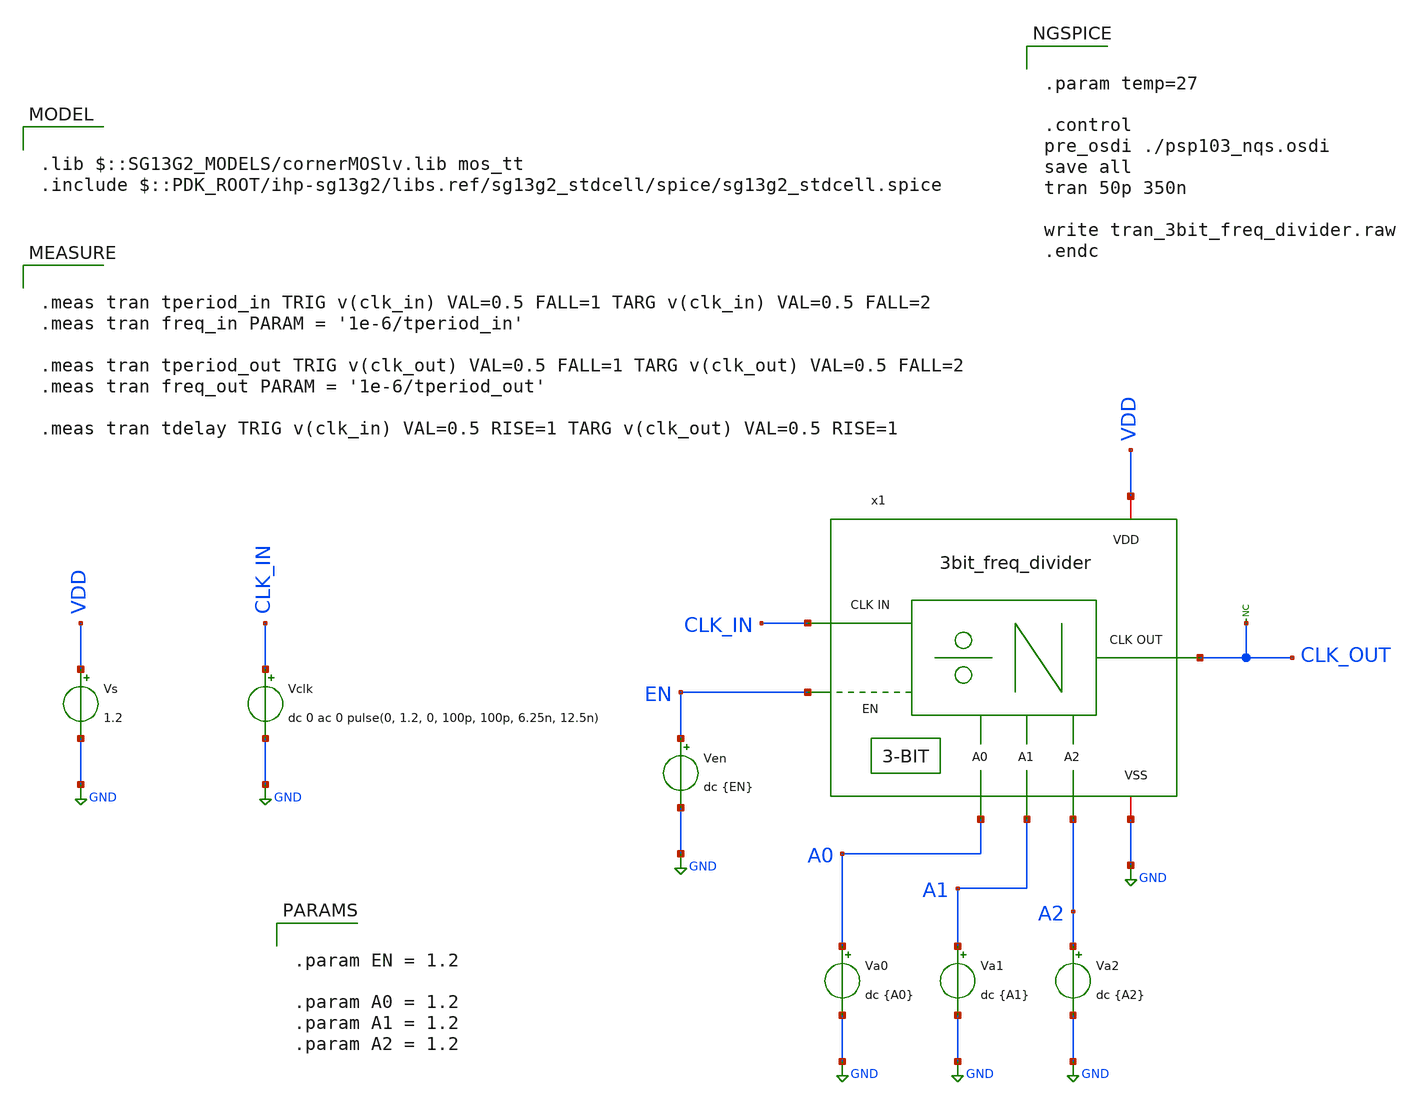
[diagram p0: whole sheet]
** sch_path: Combined Design/design_data/xschem/3bit_freq_divider_tb.sch

.lib $::SG13G2_MODELS/cornerMOSlv.lib mos_tt
.include $::PDK_ROOT/ihp-sg13g2/libs.ref/sg13g2_stdcell/spice/sg13g2_stdcell.spice

**.subckt 3bit_freq_divider_tb
Vs VDD GND 1.2
Vclk CLK_IN GND dc 0 ac 0 pulse(0, 1.2, 0, 100p, 100p, 6.25n, 12.5n)
* noconn CLK_OUT
Ven EN GND dc {EN}
Va1 A1 GND dc {A1}
Va2 A2 GND dc {A2}
x1 A0 CLK_IN EN CLK_OUT A1 VDD GND A2 3bit_freq_divider
Va0 A0 GND dc {A0}
**** begin user architecture code


.meas tran tperiod_in TRIG v(clk_in) VAL=0.5 FALL=1 TARG v(clk_in) VAL=0.5 FALL=2
.meas tran freq_in PARAM = '1e-6/tperiod_in'

.meas tran tperiod_out TRIG v(clk_out) VAL=0.5 FALL=1 TARG v(clk_out) VAL=0.5 FALL=2
.meas tran freq_out PARAM = '1e-6/tperiod_out'

.meas tran tdelay TRIG v(clk_in) VAL=0.5 RISE=1 TARG v(clk_out) VAL=0.5 RISE=1




.param EN = 1.2

.param A0 = 1.2
.param A1 = 1.2
.param A2 = 1.2




.param temp=27

.control
pre_osdi ./psp103_nqs.osdi
save all
tran 50p 350n

write tran_3bit_freq_divider.raw
.endc


**** end user architecture code
**.ends
.GLOBAL GND
.end
